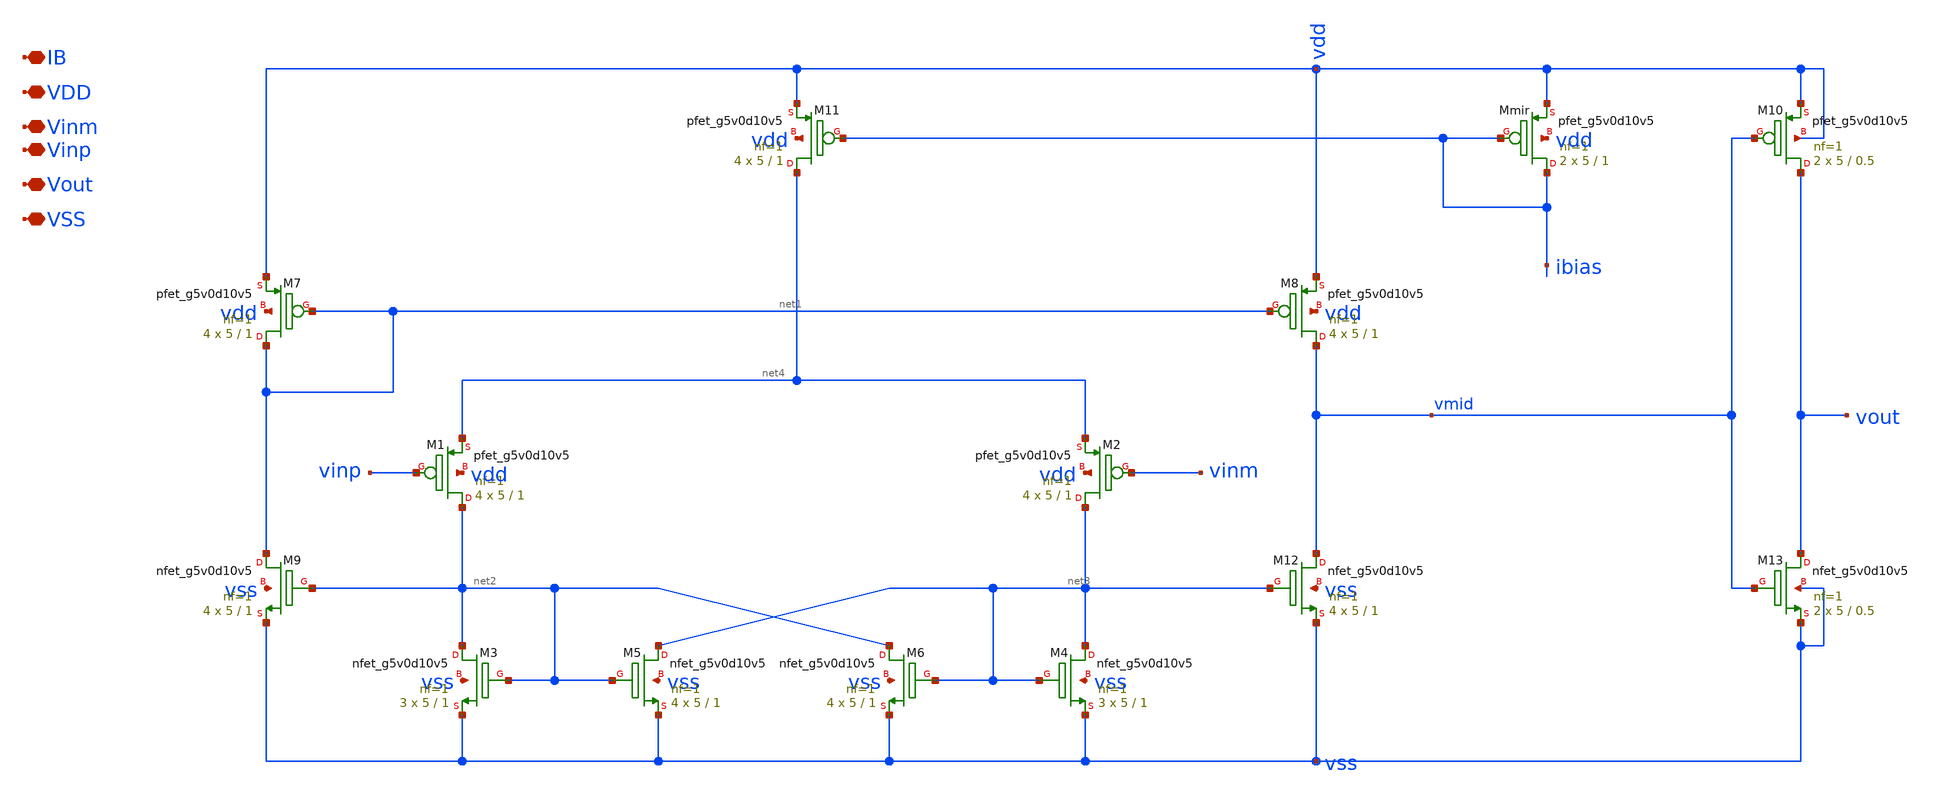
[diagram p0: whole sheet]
** sch_path: images/iic-osic-tools/addons/examples/open-pmic/design/comparator/comparator_w_obuff_and_wo_dummies.sch
**.subckt comparator_w_obuff_and_wo_dummies IB VDD Vinm Vinp Vout VSS
*.iopin IB
*.iopin VDD
*.iopin Vinm
*.iopin Vinp
*.iopin Vout
*.iopin VSS
XM1 net2 vinp net4 vdd sky130_fd_pr__pfet_g5v0d10v5 L=1 W=5 nf=1 ad='int((nf+1)/2) * W/nf * 0.29' as='int((nf+2)/2) * W/nf * 0.29'
+ pd='2*int((nf+1)/2) * (W/nf + 0.29)' ps='2*int((nf+2)/2) * (W/nf + 0.29)' nrd='0.29 / W' nrs='0.29 / W'
+ sa=0 sb=0 sd=0 mult=4 m=4
XM2 net3 vinm net4 vdd sky130_fd_pr__pfet_g5v0d10v5 L=1 W=5 nf=1 ad='int((nf+1)/2) * W/nf * 0.29' as='int((nf+2)/2) * W/nf * 0.29'
+ pd='2*int((nf+1)/2) * (W/nf + 0.29)' ps='2*int((nf+2)/2) * (W/nf + 0.29)' nrd='0.29 / W' nrs='0.29 / W'
+ sa=0 sb=0 sd=0 mult=4 m=4
XM7 net1 net1 vdd vdd sky130_fd_pr__pfet_g5v0d10v5 L=1 W=5 nf=1 ad='int((nf+1)/2) * W/nf * 0.29' as='int((nf+2)/2) * W/nf * 0.29'
+ pd='2*int((nf+1)/2) * (W/nf + 0.29)' ps='2*int((nf+2)/2) * (W/nf + 0.29)' nrd='0.29 / W' nrs='0.29 / W'
+ sa=0 sb=0 sd=0 mult=4 m=4
XM8 vmid net1 vdd vdd sky130_fd_pr__pfet_g5v0d10v5 L=1 W=5 nf=1 ad='int((nf+1)/2) * W/nf * 0.29' as='int((nf+2)/2) * W/nf * 0.29'
+ pd='2*int((nf+1)/2) * (W/nf + 0.29)' ps='2*int((nf+2)/2) * (W/nf + 0.29)' nrd='0.29 / W' nrs='0.29 / W'
+ sa=0 sb=0 sd=0 mult=4 m=4
XM11 net4 ibias vdd vdd sky130_fd_pr__pfet_g5v0d10v5 L=1 W=5 nf=1 ad='int((nf+1)/2) * W/nf * 0.29' as='int((nf+2)/2) * W/nf * 0.29'
+ pd='2*int((nf+1)/2) * (W/nf + 0.29)' ps='2*int((nf+2)/2) * (W/nf + 0.29)' nrd='0.29 / W' nrs='0.29 / W'
+ sa=0 sb=0 sd=0 mult=4 m=4
XMmir ibias ibias vdd vdd sky130_fd_pr__pfet_g5v0d10v5 L=1 W=5 nf=1 ad='int((nf+1)/2) * W/nf * 0.29'
+ as='int((nf+2)/2) * W/nf * 0.29' pd='2*int((nf+1)/2) * (W/nf + 0.29)' ps='2*int((nf+2)/2) * (W/nf + 0.29)'
+ nrd='0.29 / W' nrs='0.29 / W' sa=0 sb=0 sd=0 mult=2 m=2
XM12 vmid net3 vss vss sky130_fd_pr__nfet_g5v0d10v5 L=1 W=5 nf=1 ad='int((nf+1)/2) * W/nf * 0.29' as='int((nf+2)/2) * W/nf * 0.29'
+ pd='2*int((nf+1)/2) * (W/nf + 0.29)' ps='2*int((nf+2)/2) * (W/nf + 0.29)' nrd='0.29 / W' nrs='0.29 / W'
+ sa=0 sb=0 sd=0 mult=4 m=4
XM4 net3 net3 vss vss sky130_fd_pr__nfet_g5v0d10v5 L=1 W=5 nf=1 ad='int((nf+1)/2) * W/nf * 0.29' as='int((nf+2)/2) * W/nf * 0.29'
+ pd='2*int((nf+1)/2) * (W/nf + 0.29)' ps='2*int((nf+2)/2) * (W/nf + 0.29)' nrd='0.29 / W' nrs='0.29 / W'
+ sa=0 sb=0 sd=0 mult=3 m=3
XM6 net2 net3 vss vss sky130_fd_pr__nfet_g5v0d10v5 L=1 W=5 nf=1 ad='int((nf+1)/2) * W/nf * 0.29' as='int((nf+2)/2) * W/nf * 0.29'
+ pd='2*int((nf+1)/2) * (W/nf + 0.29)' ps='2*int((nf+2)/2) * (W/nf + 0.29)' nrd='0.29 / W' nrs='0.29 / W'
+ sa=0 sb=0 sd=0 mult=4 m=4
XM5 net3 net2 vss vss sky130_fd_pr__nfet_g5v0d10v5 L=1 W=5 nf=1 ad='int((nf+1)/2) * W/nf * 0.29' as='int((nf+2)/2) * W/nf * 0.29'
+ pd='2*int((nf+1)/2) * (W/nf + 0.29)' ps='2*int((nf+2)/2) * (W/nf + 0.29)' nrd='0.29 / W' nrs='0.29 / W'
+ sa=0 sb=0 sd=0 mult=4 m=4
XM3 net2 net2 vss vss sky130_fd_pr__nfet_g5v0d10v5 L=1 W=5 nf=1 ad='int((nf+1)/2) * W/nf * 0.29' as='int((nf+2)/2) * W/nf * 0.29'
+ pd='2*int((nf+1)/2) * (W/nf + 0.29)' ps='2*int((nf+2)/2) * (W/nf + 0.29)' nrd='0.29 / W' nrs='0.29 / W'
+ sa=0 sb=0 sd=0 mult=3 m=3
XM9 net1 net2 vss vss sky130_fd_pr__nfet_g5v0d10v5 L=1 W=5 nf=1 ad='int((nf+1)/2) * W/nf * 0.29' as='int((nf+2)/2) * W/nf * 0.29'
+ pd='2*int((nf+1)/2) * (W/nf + 0.29)' ps='2*int((nf+2)/2) * (W/nf + 0.29)' nrd='0.29 / W' nrs='0.29 / W'
+ sa=0 sb=0 sd=0 mult=4 m=4
XM10 vout vmid vdd vdd sky130_fd_pr__pfet_g5v0d10v5 L=0.5 W=5 nf=1 ad='int((nf+1)/2) * W/nf * 0.29' as='int((nf+2)/2) * W/nf * 0.29'
+ pd='2*int((nf+1)/2) * (W/nf + 0.29)' ps='2*int((nf+2)/2) * (W/nf + 0.29)' nrd='0.29 / W' nrs='0.29 / W'
+ sa=0 sb=0 sd=0 mult=2 m=2
XM13 vout vmid vss vss sky130_fd_pr__nfet_g5v0d10v5 L=0.5 W=5 nf=1 ad='int((nf+1)/2) * W/nf * 0.29' as='int((nf+2)/2) * W/nf * 0.29'
+ pd='2*int((nf+1)/2) * (W/nf + 0.29)' ps='2*int((nf+2)/2) * (W/nf + 0.29)' nrd='0.29 / W' nrs='0.29 / W'
+ sa=0 sb=0 sd=0 mult=2 m=2
**.ends
.end
